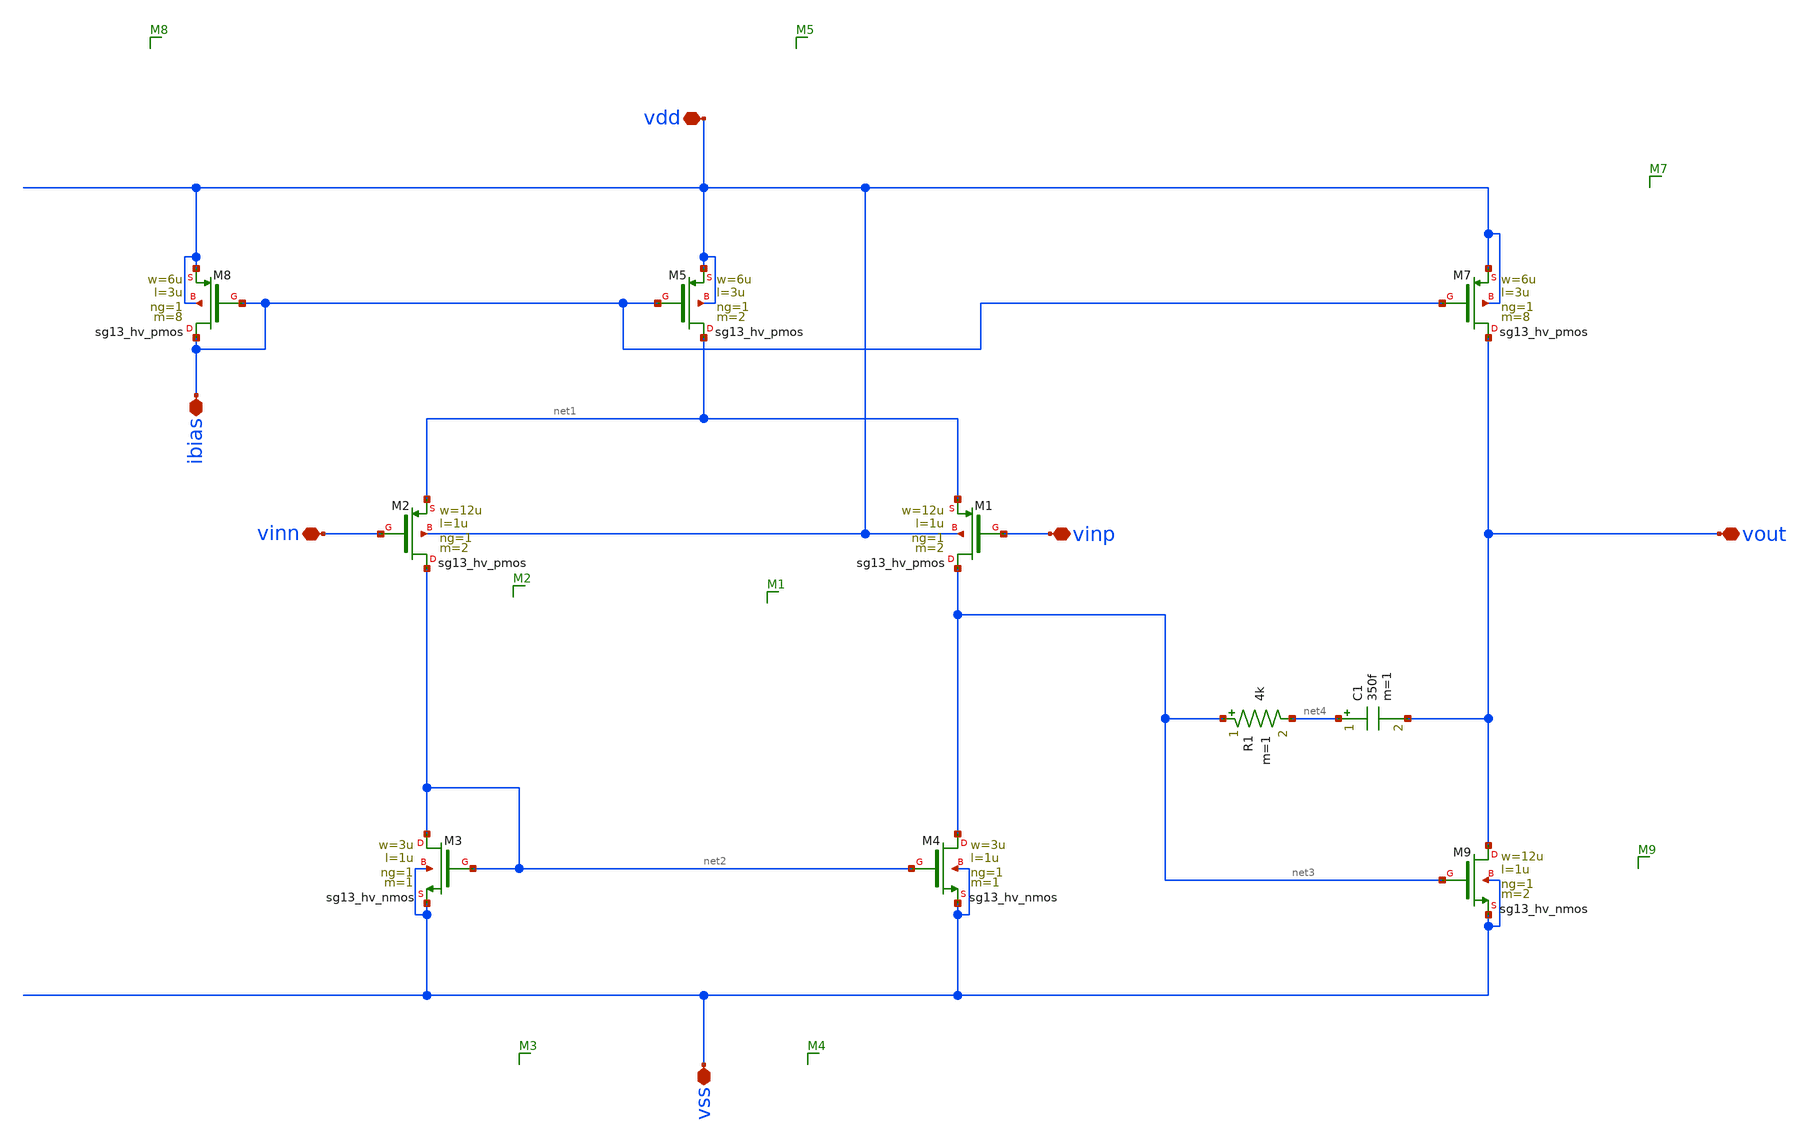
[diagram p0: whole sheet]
** sch_path: dependencies/pmu_ip/dependencies/OTA/OTA-main/testbenches/two_stage_ota_s.sch
**.subckt two_stage_ota_s ibias vdd vss vout vinp vinn
*.iopin ibias
*.iopin vdd
*.iopin vss
*.iopin vout
*.iopin vinp
*.iopin vinn
C1 net4 vout 350f m=1
R1 net3 net4 4k m=1
XM4 net3 net2 vss vss sg13_hv_nmos w=3u l=1u ng=1 m=1 mm_ok=1
XM3 net2 net2 vss vss sg13_hv_nmos w=3u l=1u ng=1 m=1 mm_ok=1
XM1 net3 vinp net1 vdd sg13_hv_pmos w=12u l=1u ng=1 m=2 mm_ok=1
XM2 net2 vinn net1 vdd sg13_hv_pmos w=12u l=1u ng=1 m=2 mm_ok=1
XM5 net1 ibias vdd vdd sg13_hv_pmos w=6u l=3u ng=1 m=2 mm_ok=1
XM7 vout ibias vdd vdd sg13_hv_pmos w=6u l=3u ng=1 m=8 mm_ok=1
XM8 ibias ibias vdd vdd sg13_hv_pmos w=6u l=3u ng=1 m=8 mm_ok=1
XM9 vout net3 vss vss sg13_hv_nmos w=12u l=1u ng=1 m=2 mm_ok=1
**.ends
.end
